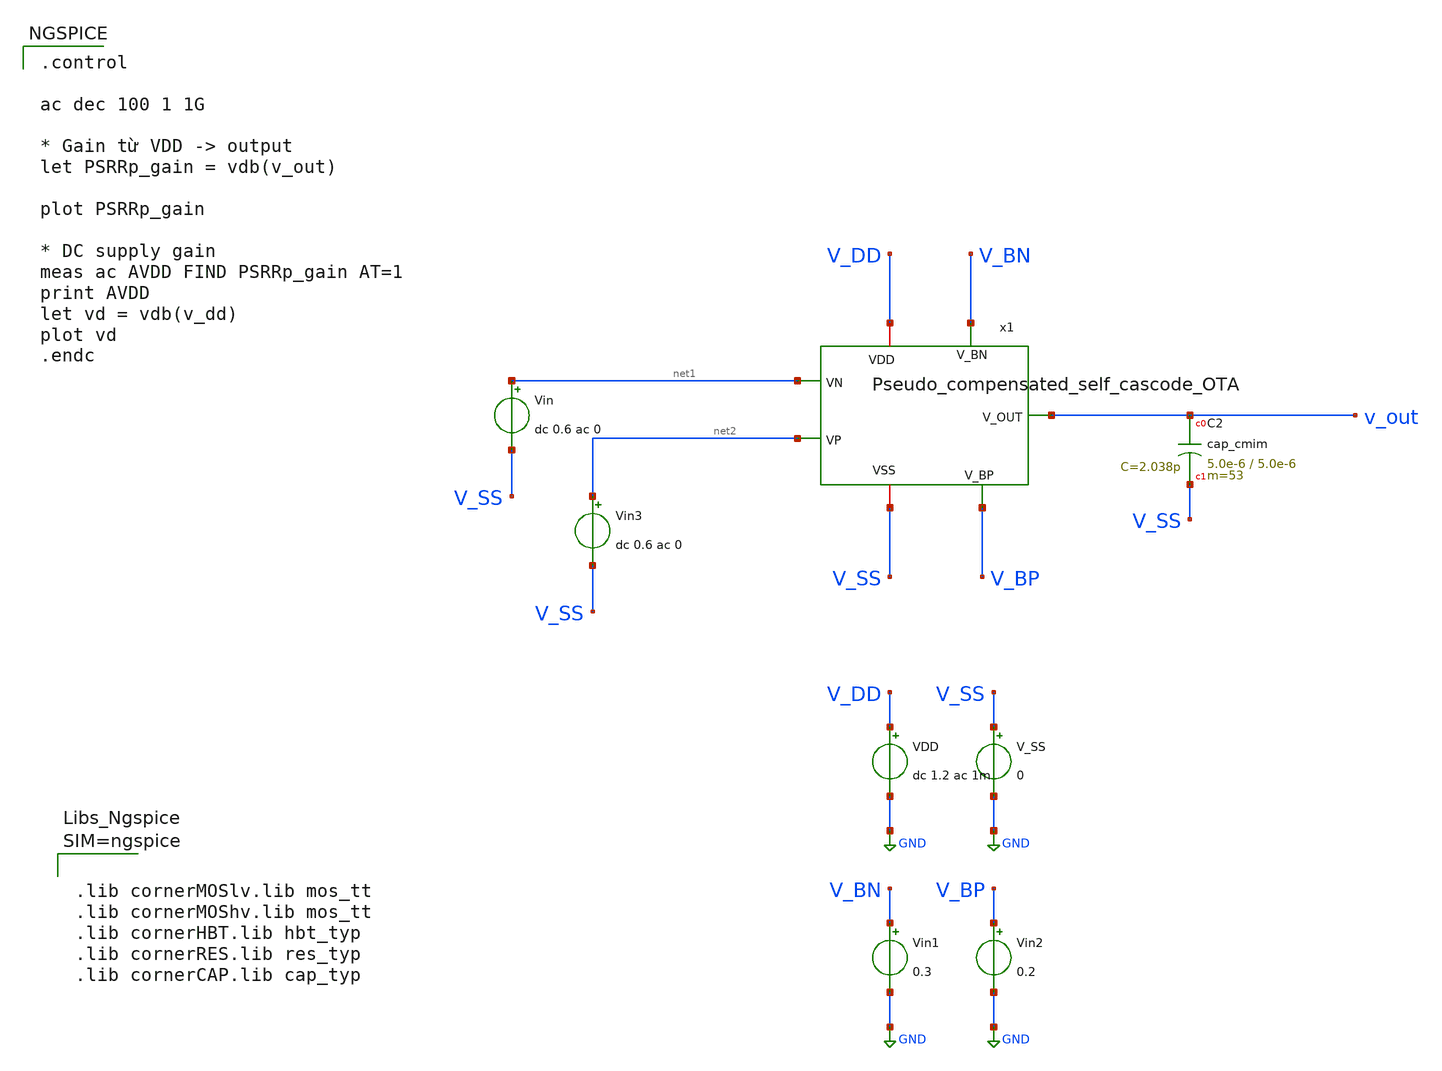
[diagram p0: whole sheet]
** sch_path: xschem/OTA_tb_psrr_p.sch
**.subckt OTA_tb_psrr_p
x1 net1 net2 V_BN V_BP v_out V_DD V_SS Pseudo_compensated_self_cascode_OTA
Vin net1 V_SS dc 0.6 ac 0
VDD V_DD GND dc 1.2 ac 1m
V_SS V_SS GND 0
Vin1 V_BN GND 0.3
Vin2 V_BP GND 0.2
Vin3 net2 V_SS dc 0.6 ac 0
XC2 v_out V_SS cap_cmim w=5.0e-6 l=5.0e-6 m=53 mm_ok=1
**** begin user architecture code

.control

ac dec 100 1 1G

* Gain từ VDD -> output
let PSRRp_gain = vdb(v_out)

plot PSRRp_gain

* DC supply gain
meas ac AVDD FIND PSRRp_gain AT=1
print AVDD
let vd = vdb(v_dd)
plot vd
.endc





.lib cornerMOSlv.lib mos_tt
.lib cornerMOShv.lib mos_tt
.lib cornerHBT.lib hbt_typ
.lib cornerRES.lib res_typ
.lib cornerCAP.lib cap_typ



**** end user architecture code
**.ends

* expanding   symbol:  Pseudo_compensated_self_cascode_OTA.sym # of pins=7
** sym_path: xschem/Pseudo_compensated_self_cascode_OTA.sym
** sch_path: xschem/Pseudo_compensated_self_cascode_OTA.sch
.subckt Pseudo_compensated_self_cascode_OTA VN VP V_BN V_BP V_OUT VDD VSS
*.ipin VN
*.ipin VP
*.ipin V_BN
*.ipin V_BP
*.opin V_OUT
*.iopin VDD
*.iopin VSS
XM11 net1 VN net2 VSS sg13_lv_nmos w=70u l=0.8u ng=7 m=1 mm_ok=1
XM12 V_GS VN net1 V_BP sg13_lv_nmos w=38.5u l=0.3u ng=4 m=1 mm_ok=1
XM21 net4 VP net2 VSS sg13_lv_nmos w=70u l=0.8u ng=7 m=1 mm_ok=1
XM22 VB32 VP net4 V_BP sg13_lv_nmos w=38.5u l=0.3u ng=4 m=1 mm_ok=1
XM52 net2 V_BN net3 V_BN sg13_lv_nmos w=40u l=0.5u ng=4 m=1 mm_ok=1
XM51 net3 V_BN VSS VSS sg13_lv_nmos w=40u l=2.5u ng=4 m=1 mm_ok=1
XM32 V_GS V_GS VS32 VB32 sg13_lv_pmos w=48.5u l=1.24u ng=5 m=1 mm_ok=1
XM31 VS32 V_GS VDD VDD sg13_lv_pmos w=48.5u l=0.87u ng=5 m=1 mm_ok=1
XM42 VB32 V_GS VS42 V_GS sg13_lv_pmos w=48.5u l=1.24u ng=5 m=1 mm_ok=1
XM41 VS42 V_GS VDD VDD sg13_lv_pmos w=48.5u l=0.87u ng=5 m=1 mm_ok=1
XM61 net5 VB32 VDD VDD sg13_lv_pmos w=60u l=0.13u ng=6 m=1 mm_ok=1
XM62 V_OUT VB32 net5 V_BP sg13_lv_pmos w=60u l=0.13u ng=6 m=1 mm_ok=1
XM72 V_OUT V_BN net6 V_BN sg13_lv_nmos w=40u l=0.5u ng=10 m=1 mm_ok=1
XM71 net6 V_BN VSS VSS sg13_lv_nmos w=40u l=2.5u ng=4 m=1 mm_ok=1
XC3 VS42 V_OUT cap_cmim w=5.0e-6 l=5.0e-6 m=38 mm_ok=1
XC1 net4 V_OUT cap_cmim w=5.0e-6 l=5.0e-6 m=38 mm_ok=1
.ends

.GLOBAL GND
.end
